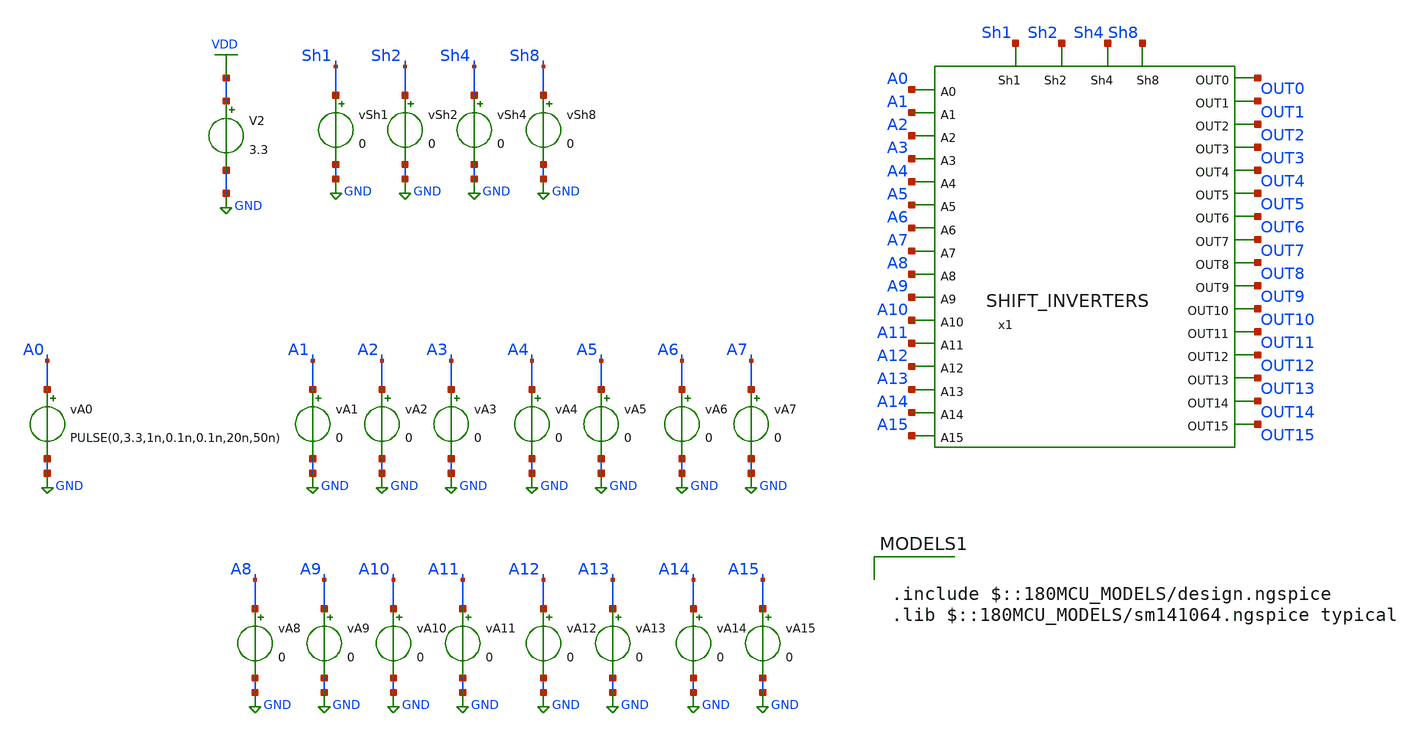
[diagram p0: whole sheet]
** sch_path: tbs/shift_rise_tb.sch
**.subckt shift_rise_tb
x1 OUT0 Sh1 OUT1 OUT2 Sh2 OUT3 OUT4 A0 OUT5 A1 OUT6 Sh4 OUT7 OUT8 A2 A3 OUT9 OUT10 OUT11 Sh8 OUT12
+ A4 OUT13 A5 A6 OUT14 A7 OUT15 A8 A9 A10 A11 A12 A13 A14 A15 SHIFT_INVERTERS
vA0 A0 GND PULSE(0,3.3,1n,0.1n,0.1n,20n,50n)
vA1 A1 GND 0
vA2 A2 GND 0
vA3 A3 GND 0
vA4 A4 GND 0
vA5 A5 GND 0
vA6 A6 GND 0
vA7 A7 GND 0
vA8 A8 GND 0
vA9 A9 GND 0
vA10 A10 GND 0
vA11 A11 GND 0
vA12 A12 GND 0
vA13 A13 GND 0
vA14 A14 GND 0
vA15 A15 GND 0
vSh1 Sh1 GND 0
vSh2 Sh2 GND 0
vSh4 Sh4 GND 0
vSh8 Sh8 GND 0
V2 VDD GND 3.3
**** begin user architecture code

.include $::180MCU_MODELS/design.ngspice
.lib $::180MCU_MODELS/sm141064.ngspice typical


.control
  set appendwrite
  shell rm -f /foss/designs/ENGN1600-CAD5/tbs/rise_results.txt

  let vlow = 0
  let vhigh = 3.3
  let tstop = 30n

  alter vSh1 = $&vhigh
  alter vSh2 = $&vlow
  alter vSh4 = $&vlow
  alter vSh8 = $&vlow
  tran 0.05n $&tstop
  meas tran tpd_rise_1 trig v(A0) val=1.65 rise=1 targ v(OUT1) val=1.65 rise=1
  shell echo tpd_rise_1 >> /foss/designs/ENGN1600-CAD5/tbs/rise_results.txt
  print tpd_rise_1 >> /foss/designs/ENGN1600-CAD5/tbs/rise_results.txt
  reset

  alter vSh1 = $&vlow
  alter vSh2 = $&vhigh
  alter vSh4 = $&vlow
  alter vSh8 = $&vlow
  tran 0.05n $&tstop
  meas tran tpd_rise_2 trig v(A0) val=1.65 rise=1 targ v(OUT2) val=1.65 rise=1
  shell echo tpd_rise_2 >> /foss/designs/ENGN1600-CAD5/tbs/rise_results.txt
  print tpd_rise_2 >> /foss/designs/ENGN1600-CAD5/tbs/rise_results.txt
  reset

  alter vSh1 = $&vhigh
  alter vSh2 = $&vhigh
  alter vSh4 = $&vlow
  alter vSh8 = $&vlow
  tran 0.05n $&tstop
  meas tran tpd_rise_3 trig v(A0) val=1.65 rise=1 targ v(OUT3) val=1.65 rise=1
  shell echo tpd_rise_3 >> /foss/designs/ENGN1600-CAD5/tbs/rise_results.txt
  print tpd_rise_3 >> /foss/designs/ENGN1600-CAD5/tbs/rise_results.txt
  reset

  alter vSh1 = $&vlow
  alter vSh2 = $&vlow
  alter vSh4 = $&vhigh
  alter vSh8 = $&vlow
  tran 0.05n $&tstop
  meas tran tpd_rise_4 trig v(A0) val=1.65 rise=1 targ v(OUT4) val=1.65 rise=1
  shell echo tpd_rise_4 >> /foss/designs/ENGN1600-CAD5/tbs/rise_results.txt
  print tpd_rise_4 >> /foss/designs/ENGN1600-CAD5/tbs/rise_results.txt
  reset

  alter vSh1 = $&vhigh
  alter vSh2 = $&vlow
  alter vSh4 = $&vhigh
  alter vSh8 = $&vlow
  tran 0.05n $&tstop
  meas tran tpd_rise_5 trig v(A0) val=1.65 rise=1 targ v(OUT5) val=1.65 rise=1
  shell echo tpd_rise_5 >> /foss/designs/ENGN1600-CAD5/tbs/rise_results.txt
  print tpd_rise_5 >> /foss/designs/ENGN1600-CAD5/tbs/rise_results.txt
  reset

  alter vSh1 = $&vlow
  alter vSh2 = $&vhigh
  alter vSh4 = $&vhigh
  alter vSh8 = $&vlow
  tran 0.05n $&tstop
  meas tran tpd_rise_6 trig v(A0) val=1.65 rise=1 targ v(OUT6) val=1.65 rise=1
  shell echo tpd_rise_6 >> /foss/designs/ENGN1600-CAD5/tbs/rise_results.txt
  print tpd_rise_6 >> /foss/designs/ENGN1600-CAD5/tbs/rise_results.txt
  reset

  alter vSh1 = $&vhigh
  alter vSh2 = $&vhigh
  alter vSh4 = $&vhigh
  alter vSh8 = $&vlow
  tran 0.05n $&tstop
  meas tran tpd_rise_7 trig v(A0) val=1.65 rise=1 targ v(OUT7) val=1.65 rise=1
  shell echo tpd_rise_7 >> /foss/designs/ENGN1600-CAD5/tbs/rise_results.txt
  print tpd_rise_7 >> /foss/designs/ENGN1600-CAD5/tbs/rise_results.txt
  reset

  alter vSh1 = $&vlow
  alter vSh2 = $&vlow
  alter vSh4 = $&vlow
  alter vSh8 = $&vhigh
  tran 0.05n $&tstop
  meas tran tpd_rise_8 trig v(A0) val=1.65 rise=1 targ v(OUT8) val=1.65 rise=1
  shell echo tpd_rise_8 >> /foss/designs/ENGN1600-CAD5/tbs/rise_results.txt
  print tpd_rise_8 >> /foss/designs/ENGN1600-CAD5/tbs/rise_results.txt
  reset

  alter vSh1 = $&vhigh
  alter vSh2 = $&vlow
  alter vSh4 = $&vlow
  alter vSh8 = $&vhigh
  tran 0.05n $&tstop
  meas tran tpd_rise_9 trig v(A0) val=1.65 rise=1 targ v(OUT9) val=1.65 rise=1
  shell echo tpd_rise_9 >> /foss/designs/ENGN1600-CAD5/tbs/rise_results.txt
  print tpd_rise_9 >> /foss/designs/ENGN1600-CAD5/tbs/rise_results.txt
  reset

  alter vSh1 = $&vlow
  alter vSh2 = $&vhigh
  alter vSh4 = $&vlow
  alter vSh8 = $&vhigh
  tran 0.05n $&tstop
  meas tran tpd_rise_10 trig v(A0) val=1.65 rise=1 targ v(OUT10) val=1.65 rise=1
  shell echo tpd_rise_10 >> /foss/designs/ENGN1600-CAD5/tbs/rise_results.txt
  print tpd_rise_10 >> /foss/designs/ENGN1600-CAD5/tbs/rise_results.txt
  reset

  alter vSh1 = $&vhigh
  alter vSh2 = $&vhigh
  alter vSh4 = $&vlow
  alter vSh8 = $&vhigh
  tran 0.05n $&tstop
  meas tran tpd_rise_11 trig v(A0) val=1.65 rise=1 targ v(OUT11) val=1.65 rise=1
  shell echo tpd_rise_11 >> /foss/designs/ENGN1600-CAD5/tbs/rise_results.txt
  print tpd_rise_11 >> /foss/designs/ENGN1600-CAD5/tbs/rise_results.txt
  reset

  alter vSh1 = $&vlow
  alter vSh2 = $&vlow
  alter vSh4 = $&vhigh
  alter vSh8 = $&vhigh
  tran 0.05n $&tstop
  meas tran tpd_rise_12 trig v(A0) val=1.65 rise=1 targ v(OUT12) val=1.65 rise=1
  shell echo tpd_rise_12 >> /foss/designs/ENGN1600-CAD5/tbs/rise_results.txt
  print tpd_rise_12 >> /foss/designs/ENGN1600-CAD5/tbs/rise_results.txt
  reset

  alter vSh1 = $&vhigh
  alter vSh2 = $&vlow
  alter vSh4 = $&vhigh
  alter vSh8 = $&vhigh
  tran 0.05n $&tstop
  meas tran tpd_rise_13 trig v(A0) val=1.65 rise=1 targ v(OUT13) val=1.65 rise=1
  shell echo tpd_rise_13 >> /foss/designs/ENGN1600-CAD5/tbs/rise_results.txt
  print tpd_rise_13 >> /foss/designs/ENGN1600-CAD5/tbs/rise_results.txt
  reset

  alter vSh1 = $&vlow
  alter vSh2 = $&vhigh
  alter vSh4 = $&vhigh
  alter vSh8 = $&vhigh
  tran 0.05n $&tstop
  meas tran tpd_rise_14 trig v(A0) val=1.65 rise=1 targ v(OUT14) val=1.65 rise=1
  shell echo tpd_rise_14 >> /foss/designs/ENGN1600-CAD5/tbs/rise_results.txt
  print tpd_rise_14 >> /foss/designs/ENGN1600-CAD5/tbs/rise_results.txt
  reset

  alter vSh1 = $&vhigh
  alter vSh2 = $&vhigh
  alter vSh4 = $&vhigh
  alter vSh8 = $&vhigh
  tran 0.05n $&tstop
  meas tran tpd_rise_15 trig v(A0) val=1.65 rise=1 targ v(OUT15) val=1.65 rise=1
  shell echo tpd_rise_15 >> /foss/designs/ENGN1600-CAD5/tbs/rise_results.txt
  print tpd_rise_15 >> /foss/designs/ENGN1600-CAD5/tbs/rise_results.txt
.endc


**** end user architecture code
**.ends
.GLOBAL GND
.GLOBAL VDD
.end
